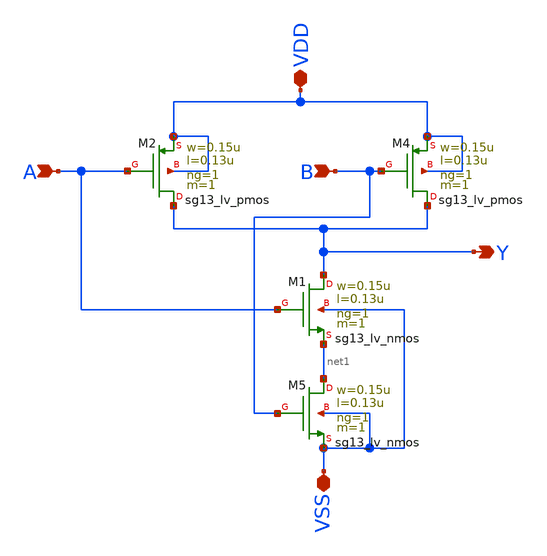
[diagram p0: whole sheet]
** sch_path: logic_gate/NAND2/Layout_Post-Simulation/NAND2.sch
**.subckt NAND2 VDD VSS A Y B
*.iopin VDD
*.iopin VSS
*.ipin A
*.opin Y
*.ipin B
XM1 Y A net1 VSS sg13_lv_nmos w=0.15u l=0.13u ng=1 m=1 mm_ok=1
XM2 Y A VDD VDD sg13_lv_pmos w=0.15u l=0.13u ng=1 m=1 mm_ok=1
XM4 Y B VDD VDD sg13_lv_pmos w=0.15u l=0.13u ng=1 m=1 mm_ok=1
XM5 net1 B VSS VSS sg13_lv_nmos w=0.15u l=0.13u ng=1 m=1 mm_ok=1
**.ends
.end
